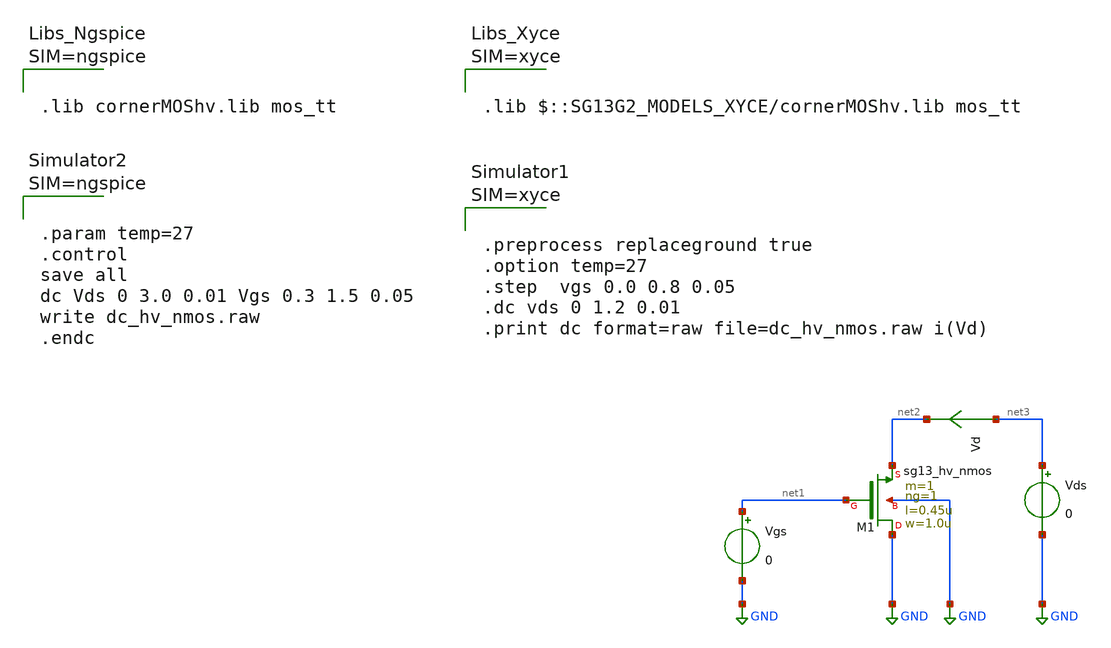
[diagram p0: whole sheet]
** sch_path: ihp-sg13g2/libs.tech/xschem/sg13g2_tests_xyce/dc_hv_nmos.sch
* Copyright 2023 IHP PDK Authors
**.subckt dc_hv_nmos
Vgs net1 GND 0
Vds net3 GND 0
Vd net3 net2 0
.save i(vd)
XM1 GND net1 net2 GND sg13_hv_nmos w=1.0u l=0.45u ng=1 m=1 mm_ok=1
**** begin user architecture code









.lib cornerMOShv.lib mos_tt






.param temp=27
.control
save all
dc Vds 0 3.0 0.01 Vgs 0.3 1.5 0.05
write dc_hv_nmos.raw
.endc



**** end user architecture code
**.ends
.GLOBAL GND
.end
